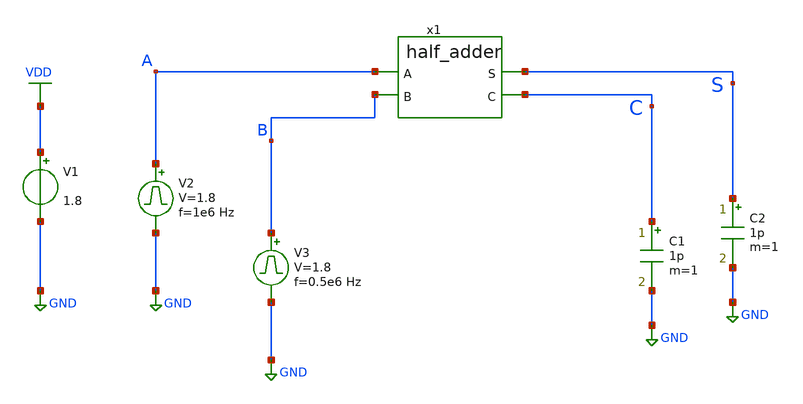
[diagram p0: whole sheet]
** sch_path: circuits/xschem/half_adder_tb.sch
**.subckt half_adder_tb
V1 VDD GND 1.8
V2 A GND pulse 0 1.8 '0.495/ 1e6 ' '0.01/1e6 ' '0.01/1e6 ' '0.49/1e6 ' '1/1e6 '
C1 C GND 1p m=1
V3 B GND pulse 0 1.8 '0.495/ 0.5e6 ' '0.01/0.5e6 ' '0.01/0.5e6 ' '0.49/0.5e6 ' '1/0.5e6 '
x1 A S B C half_adder
C2 S GND 1p m=1
**** begin user architecture code


.control
save all
tran 1n 2u
plot V(A) V(B)+2 V(S)+4 V(C)+6
.endc



** opencircuitdesign pdks install
.lib $::SKYWATER_MODELS/sky130.lib.spice tt


**** end user architecture code
**.ends
.GLOBAL VDD
.GLOBAL GND
.end
